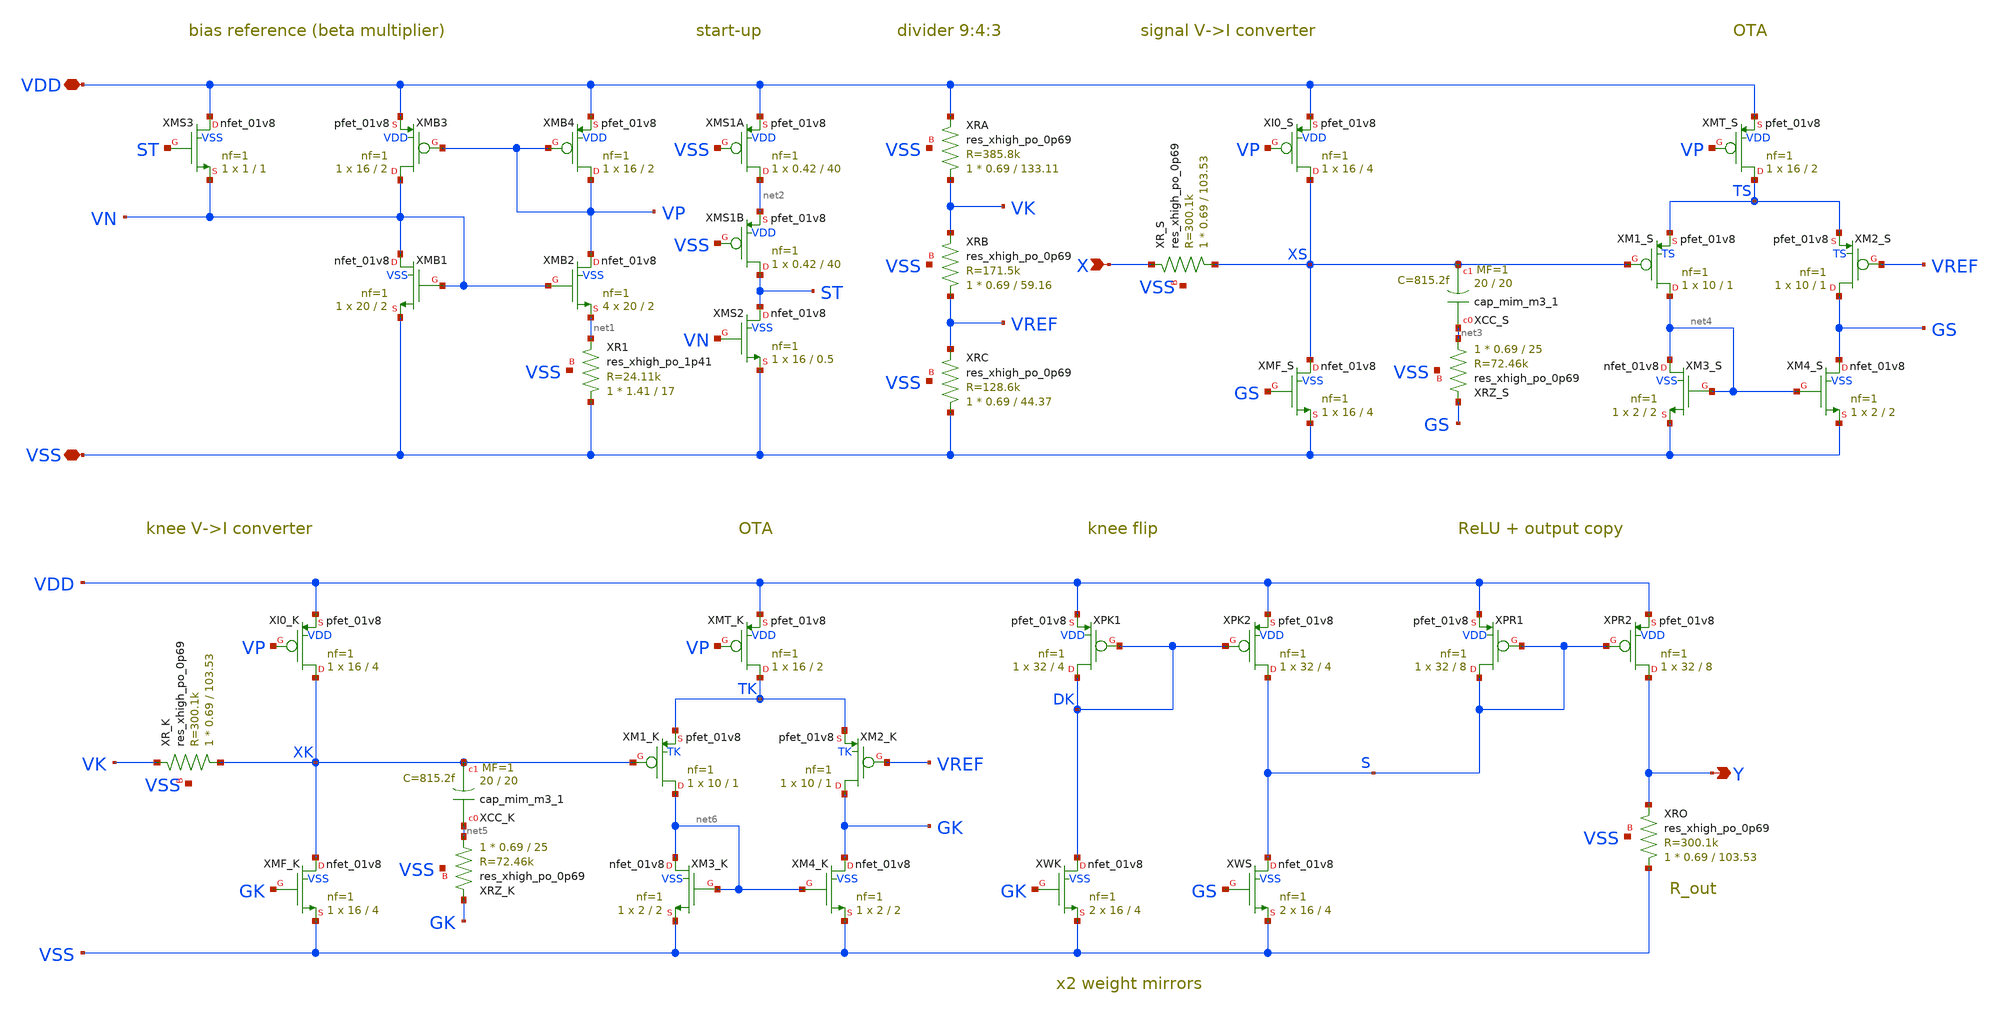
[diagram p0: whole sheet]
** sch_path: xschem/analog_neuron.sch
**.subckt analog_neuron X Y VDD VSS
*.ipin X
*.opin Y
*.iopin VDD
*.iopin VSS
XXMS3 VDD ST VN VSS sky130_fd_pr__nfet_01v8 L=1 W=1 nf=1 ad='int((nf+1)/2) * W/nf * 0.29' as='int((nf+2)/2) * W/nf * 0.29'
+ pd='2*int((nf+1)/2) * (W/nf + 0.29)' ps='2*int((nf+2)/2) * (W/nf + 0.29)' nrd='0.29 / W' nrs='0.29 / W'
+ sa=0 sb=0 sd=0 mult=1 m=1
XXMB3 VN VP VDD VDD sky130_fd_pr__pfet_01v8 L=2 W=16 nf=1 ad='int((1 + 1)/2) * 16 / 1 * 0.29' as='int((1 + 2)/2) * 16 / 1 * 0.29'
+ pd='2*int((1 + 1)/2) * (16 / 1 + 0.29)' ps='2*int((1 + 2)/2) * (16 / 1 + 0.29)' nrd='0.29 / 16 ' nrs='0.29 / 16 '
+ sa=0 sb=0 sd=0 mult=1 m=1
XXMB4 VP VP VDD VDD sky130_fd_pr__pfet_01v8 L=2 W=16 nf=1 ad='int((1 + 1)/2) * 16 / 1 * 0.29' as='int((1 + 2)/2) * 16 / 1 * 0.29'
+ pd='2*int((1 + 1)/2) * (16 / 1 + 0.29)' ps='2*int((1 + 2)/2) * (16 / 1 + 0.29)' nrd='0.29 / 16 ' nrs='0.29 / 16 '
+ sa=0 sb=0 sd=0 mult=1 m=1
XXMB1 VN VN VSS VSS sky130_fd_pr__nfet_01v8 L=2 W=20 nf=1 ad='int((nf+1)/2) * W/nf * 0.29' as='int((nf+2)/2) * W/nf * 0.29'
+ pd='2*int((nf+1)/2) * (W/nf + 0.29)' ps='2*int((nf+2)/2) * (W/nf + 0.29)' nrd='0.29 / W' nrs='0.29 / W'
+ sa=0 sb=0 sd=0 mult=1 m=1
XXMB2 VP VN net1 VSS sky130_fd_pr__nfet_01v8 L=2 W=20 nf=1 ad='int((nf+1)/2) * W/nf * 0.29' as='int((nf+2)/2) * W/nf * 0.29'
+ pd='2*int((nf+1)/2) * (W/nf + 0.29)' ps='2*int((nf+2)/2) * (W/nf + 0.29)' nrd='0.29 / W' nrs='0.29 / W'
+ sa=0 sb=0 sd=0 mult=4 m=4
XXR1 VSS net1 VSS sky130_fd_pr__res_xhigh_po_1p41 L=17 mult=1 m=1
XXMS1A net2 VSS VDD VDD sky130_fd_pr__pfet_01v8 L=40 W=0.42 nf=1 ad='int((1 + 1)/2) * 0.42 / 1 * 0.29'
+ as='int((1 + 2)/2) * 0.42 / 1 * 0.29' pd='2*int((1 + 1)/2) * (0.42 / 1 + 0.29)' ps='2*int((1 + 2)/2) * (0.42 / 1 + 0.29)'
+ nrd='0.29 / 0.42 ' nrs='0.29 / 0.42 ' sa=0 sb=0 sd=0 mult=1 m=1
XXMS1B ST VSS net2 VDD sky130_fd_pr__pfet_01v8 L=40 W=0.42 nf=1 ad='int((1 + 1)/2) * 0.42 / 1 * 0.29'
+ as='int((1 + 2)/2) * 0.42 / 1 * 0.29' pd='2*int((1 + 1)/2) * (0.42 / 1 + 0.29)' ps='2*int((1 + 2)/2) * (0.42 / 1 + 0.29)'
+ nrd='0.29 / 0.42 ' nrs='0.29 / 0.42 ' sa=0 sb=0 sd=0 mult=1 m=1
XXMS2 ST VN VSS VSS sky130_fd_pr__nfet_01v8 L=0.5 W=16 nf=1 ad='int((nf+1)/2) * W/nf * 0.29' as='int((nf+2)/2) * W/nf * 0.29'
+ pd='2*int((nf+1)/2) * (W/nf + 0.29)' ps='2*int((nf+2)/2) * (W/nf + 0.29)' nrd='0.29 / W' nrs='0.29 / W'
+ sa=0 sb=0 sd=0 mult=1 m=1
XXRA VK VDD VSS sky130_fd_pr__res_xhigh_po_0p69 L=133.11 mult=1 m=1
XXRB VREF VK VSS sky130_fd_pr__res_xhigh_po_0p69 L=59.16 mult=1 m=1
XXRC VSS VREF VSS sky130_fd_pr__res_xhigh_po_0p69 L=44.37 mult=1 m=1
XXR_S XS X VSS sky130_fd_pr__res_xhigh_po_0p69 L=103.53 mult=1 m=1
XXI0_S XS VP VDD VDD sky130_fd_pr__pfet_01v8 L=4 W=16 nf=1 ad='int((1 + 1)/2) * 16 / 1 * 0.29' as='int((1 + 2)/2) * 16 / 1 * 0.29'
+ pd='2*int((1 + 1)/2) * (16 / 1 + 0.29)' ps='2*int((1 + 2)/2) * (16 / 1 + 0.29)' nrd='0.29 / 16 ' nrs='0.29 / 16 '
+ sa=0 sb=0 sd=0 mult=1 m=1
XXMF_S XS GS VSS VSS sky130_fd_pr__nfet_01v8 L=4 W=16 nf=1 ad='int((nf+1)/2) * W/nf * 0.29' as='int((nf+2)/2) * W/nf * 0.29'
+ pd='2*int((nf+1)/2) * (W/nf + 0.29)' ps='2*int((nf+2)/2) * (W/nf + 0.29)' nrd='0.29 / W' nrs='0.29 / W'
+ sa=0 sb=0 sd=0 mult=1 m=1
XXCC_S net3 XS sky130_fd_pr__cap_mim_m3_1 W=20 L=20 MF=1 m=1
XXRZ_S net3 GS VSS sky130_fd_pr__res_xhigh_po_0p69 L=25 mult=1 m=1
XXMT_S TS VP VDD VDD sky130_fd_pr__pfet_01v8 L=2 W=16 nf=1 ad='int((1 + 1)/2) * 16 / 1 * 0.29' as='int((1 + 2)/2) * 16 / 1 * 0.29'
+ pd='2*int((1 + 1)/2) * (16 / 1 + 0.29)' ps='2*int((1 + 2)/2) * (16 / 1 + 0.29)' nrd='0.29 / 16 ' nrs='0.29 / 16 '
+ sa=0 sb=0 sd=0 mult=1 m=1
XXM1_S net4 XS TS TS sky130_fd_pr__pfet_01v8 L=1 W=10 nf=1 ad='int((1 + 1)/2) * 10 / 1 * 0.29' as='int((1 + 2)/2) * 10 / 1 * 0.29'
+ pd='2*int((1 + 1)/2) * (10 / 1 + 0.29)' ps='2*int((1 + 2)/2) * (10 / 1 + 0.29)' nrd='0.29 / 10 ' nrs='0.29 / 10 '
+ sa=0 sb=0 sd=0 mult=1 m=1
XXM2_S GS VREF TS TS sky130_fd_pr__pfet_01v8 L=1 W=10 nf=1 ad='int((1 + 1)/2) * 10 / 1 * 0.29' as='int((1 + 2)/2) * 10 / 1 * 0.29'
+ pd='2*int((1 + 1)/2) * (10 / 1 + 0.29)' ps='2*int((1 + 2)/2) * (10 / 1 + 0.29)' nrd='0.29 / 10 ' nrs='0.29 / 10 '
+ sa=0 sb=0 sd=0 mult=1 m=1
XXM3_S net4 net4 VSS VSS sky130_fd_pr__nfet_01v8 L=2 W=2 nf=1 ad='int((nf+1)/2) * W/nf * 0.29' as='int((nf+2)/2) * W/nf * 0.29'
+ pd='2*int((nf+1)/2) * (W/nf + 0.29)' ps='2*int((nf+2)/2) * (W/nf + 0.29)' nrd='0.29 / W' nrs='0.29 / W'
+ sa=0 sb=0 sd=0 mult=1 m=1
XXM4_S GS net4 VSS VSS sky130_fd_pr__nfet_01v8 L=2 W=2 nf=1 ad='int((nf+1)/2) * W/nf * 0.29' as='int((nf+2)/2) * W/nf * 0.29'
+ pd='2*int((nf+1)/2) * (W/nf + 0.29)' ps='2*int((nf+2)/2) * (W/nf + 0.29)' nrd='0.29 / W' nrs='0.29 / W'
+ sa=0 sb=0 sd=0 mult=1 m=1
XXR_K XK VK VSS sky130_fd_pr__res_xhigh_po_0p69 L=103.53 mult=1 m=1
XXI0_K XK VP VDD VDD sky130_fd_pr__pfet_01v8 L=4 W=16 nf=1 ad='int((1 + 1)/2) * 16 / 1 * 0.29' as='int((1 + 2)/2) * 16 / 1 * 0.29'
+ pd='2*int((1 + 1)/2) * (16 / 1 + 0.29)' ps='2*int((1 + 2)/2) * (16 / 1 + 0.29)' nrd='0.29 / 16 ' nrs='0.29 / 16 '
+ sa=0 sb=0 sd=0 mult=1 m=1
XXMF_K XK GK VSS VSS sky130_fd_pr__nfet_01v8 L=4 W=16 nf=1 ad='int((nf+1)/2) * W/nf * 0.29' as='int((nf+2)/2) * W/nf * 0.29'
+ pd='2*int((nf+1)/2) * (W/nf + 0.29)' ps='2*int((nf+2)/2) * (W/nf + 0.29)' nrd='0.29 / W' nrs='0.29 / W'
+ sa=0 sb=0 sd=0 mult=1 m=1
XXCC_K net5 XK sky130_fd_pr__cap_mim_m3_1 W=20 L=20 MF=1 m=1
XXRZ_K net5 GK VSS sky130_fd_pr__res_xhigh_po_0p69 L=25 mult=1 m=1
XXMT_K TK VP VDD VDD sky130_fd_pr__pfet_01v8 L=2 W=16 nf=1 ad='int((1 + 1)/2) * 16 / 1 * 0.29' as='int((1 + 2)/2) * 16 / 1 * 0.29'
+ pd='2*int((1 + 1)/2) * (16 / 1 + 0.29)' ps='2*int((1 + 2)/2) * (16 / 1 + 0.29)' nrd='0.29 / 16 ' nrs='0.29 / 16 '
+ sa=0 sb=0 sd=0 mult=1 m=1
XXM1_K net6 XK TK TK sky130_fd_pr__pfet_01v8 L=1 W=10 nf=1 ad='int((1 + 1)/2) * 10 / 1 * 0.29' as='int((1 + 2)/2) * 10 / 1 * 0.29'
+ pd='2*int((1 + 1)/2) * (10 / 1 + 0.29)' ps='2*int((1 + 2)/2) * (10 / 1 + 0.29)' nrd='0.29 / 10 ' nrs='0.29 / 10 '
+ sa=0 sb=0 sd=0 mult=1 m=1
XXM2_K GK VREF TK TK sky130_fd_pr__pfet_01v8 L=1 W=10 nf=1 ad='int((1 + 1)/2) * 10 / 1 * 0.29' as='int((1 + 2)/2) * 10 / 1 * 0.29'
+ pd='2*int((1 + 1)/2) * (10 / 1 + 0.29)' ps='2*int((1 + 2)/2) * (10 / 1 + 0.29)' nrd='0.29 / 10 ' nrs='0.29 / 10 '
+ sa=0 sb=0 sd=0 mult=1 m=1
XXM3_K net6 net6 VSS VSS sky130_fd_pr__nfet_01v8 L=2 W=2 nf=1 ad='int((nf+1)/2) * W/nf * 0.29' as='int((nf+2)/2) * W/nf * 0.29'
+ pd='2*int((nf+1)/2) * (W/nf + 0.29)' ps='2*int((nf+2)/2) * (W/nf + 0.29)' nrd='0.29 / W' nrs='0.29 / W'
+ sa=0 sb=0 sd=0 mult=1 m=1
XXM4_K GK net6 VSS VSS sky130_fd_pr__nfet_01v8 L=2 W=2 nf=1 ad='int((nf+1)/2) * W/nf * 0.29' as='int((nf+2)/2) * W/nf * 0.29'
+ pd='2*int((nf+1)/2) * (W/nf + 0.29)' ps='2*int((nf+2)/2) * (W/nf + 0.29)' nrd='0.29 / W' nrs='0.29 / W'
+ sa=0 sb=0 sd=0 mult=1 m=1
XXPK1 DK DK VDD VDD sky130_fd_pr__pfet_01v8 L=4 W=32 nf=1 ad='int((1 + 1)/2) * 32 / 1 * 0.29' as='int((1 + 2)/2) * 32 / 1 * 0.29'
+ pd='2*int((1 + 1)/2) * (32 / 1 + 0.29)' ps='2*int((1 + 2)/2) * (32 / 1 + 0.29)' nrd='0.29 / 32 ' nrs='0.29 / 32 '
+ sa=0 sb=0 sd=0 mult=1 m=1
XXPK2 S DK VDD VDD sky130_fd_pr__pfet_01v8 L=4 W=32 nf=1 ad='int((1 + 1)/2) * 32 / 1 * 0.29' as='int((1 + 2)/2) * 32 / 1 * 0.29'
+ pd='2*int((1 + 1)/2) * (32 / 1 + 0.29)' ps='2*int((1 + 2)/2) * (32 / 1 + 0.29)' nrd='0.29 / 32 ' nrs='0.29 / 32 '
+ sa=0 sb=0 sd=0 mult=1 m=1
XXWK DK GK VSS VSS sky130_fd_pr__nfet_01v8 L=4 W=16 nf=1 ad='int((nf+1)/2) * W/nf * 0.29' as='int((nf+2)/2) * W/nf * 0.29'
+ pd='2*int((nf+1)/2) * (W/nf + 0.29)' ps='2*int((nf+2)/2) * (W/nf + 0.29)' nrd='0.29 / W' nrs='0.29 / W'
+ sa=0 sb=0 sd=0 mult=2 m=2
XXWS S GS VSS VSS sky130_fd_pr__nfet_01v8 L=4 W=16 nf=1 ad='int((nf+1)/2) * W/nf * 0.29' as='int((nf+2)/2) * W/nf * 0.29'
+ pd='2*int((nf+1)/2) * (W/nf + 0.29)' ps='2*int((nf+2)/2) * (W/nf + 0.29)' nrd='0.29 / W' nrs='0.29 / W'
+ sa=0 sb=0 sd=0 mult=2 m=2
XXPR1 S S VDD VDD sky130_fd_pr__pfet_01v8 L=8 W=32 nf=1 ad='int((1 + 1)/2) * 32 / 1 * 0.29' as='int((1 + 2)/2) * 32 / 1 * 0.29'
+ pd='2*int((1 + 1)/2) * (32 / 1 + 0.29)' ps='2*int((1 + 2)/2) * (32 / 1 + 0.29)' nrd='0.29 / 32 ' nrs='0.29 / 32 '
+ sa=0 sb=0 sd=0 mult=1 m=1
XXPR2 Y S VDD VDD sky130_fd_pr__pfet_01v8 L=8 W=32 nf=1 ad='int((1 + 1)/2) * 32 / 1 * 0.29' as='int((1 + 2)/2) * 32 / 1 * 0.29'
+ pd='2*int((1 + 1)/2) * (32 / 1 + 0.29)' ps='2*int((1 + 2)/2) * (32 / 1 + 0.29)' nrd='0.29 / 32 ' nrs='0.29 / 32 '
+ sa=0 sb=0 sd=0 mult=1 m=1
XXRO VSS Y VSS sky130_fd_pr__res_xhigh_po_0p69 L=103.53 mult=1 m=1
**.ends
.end
